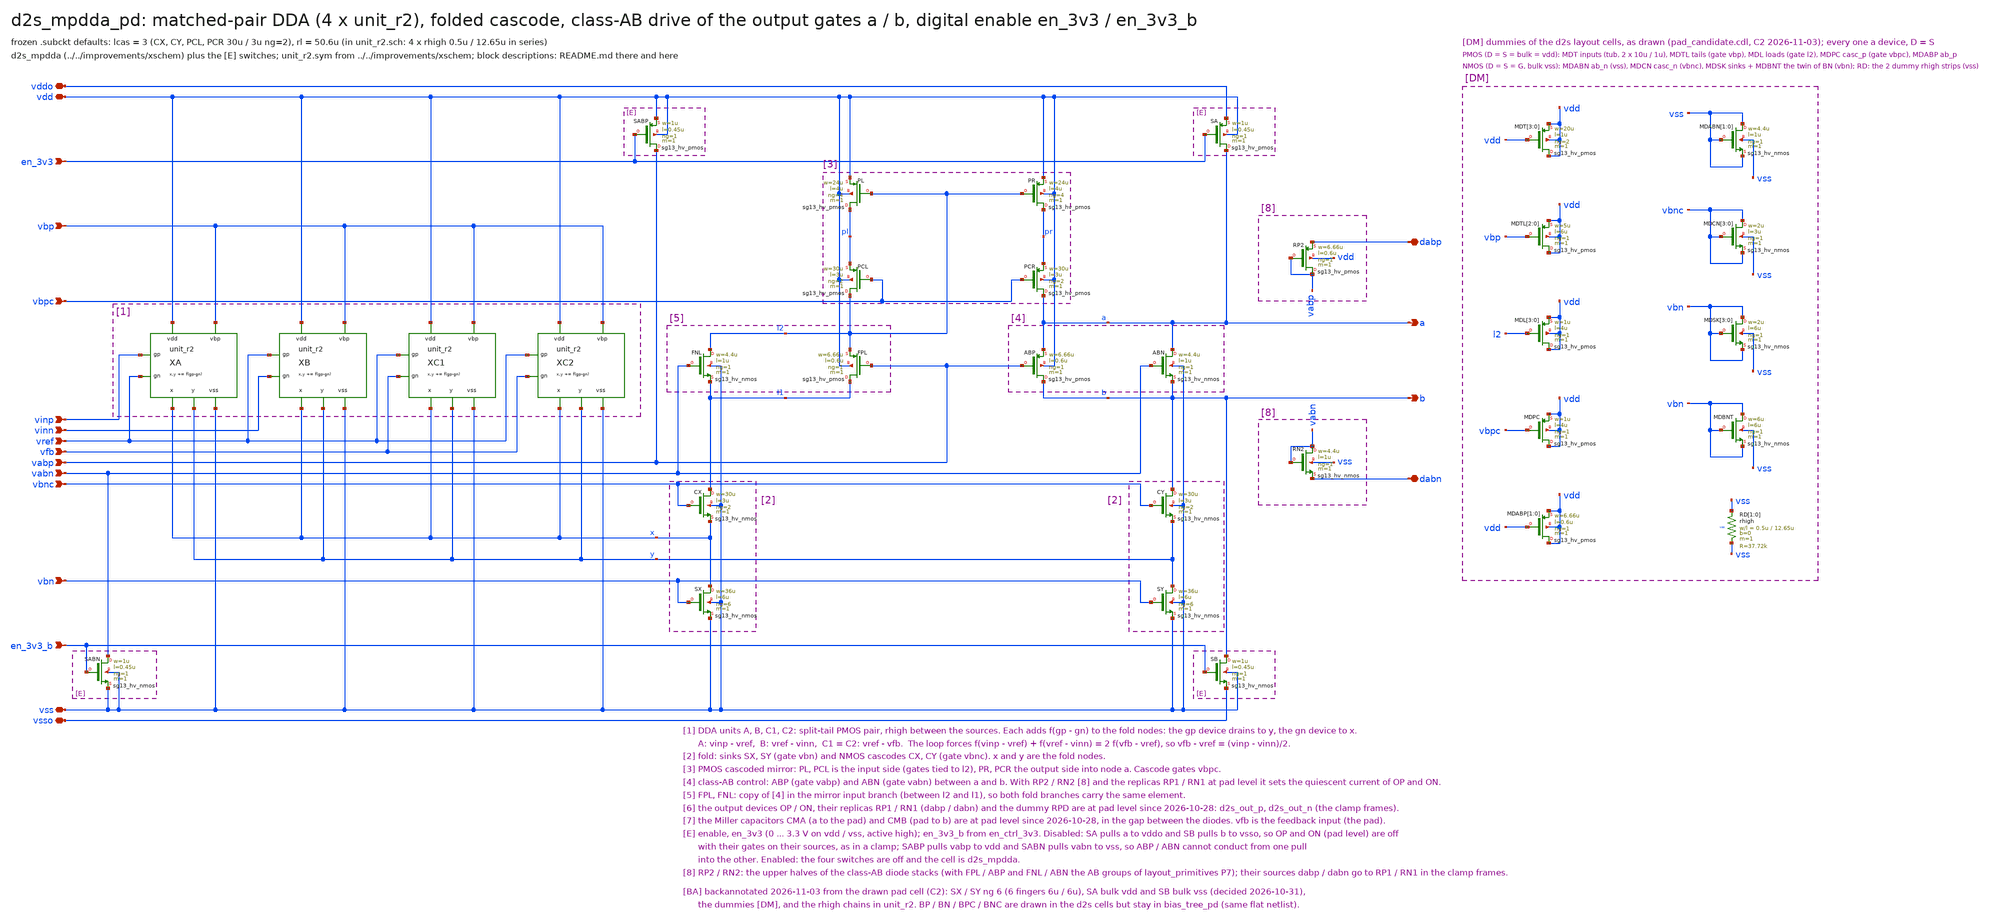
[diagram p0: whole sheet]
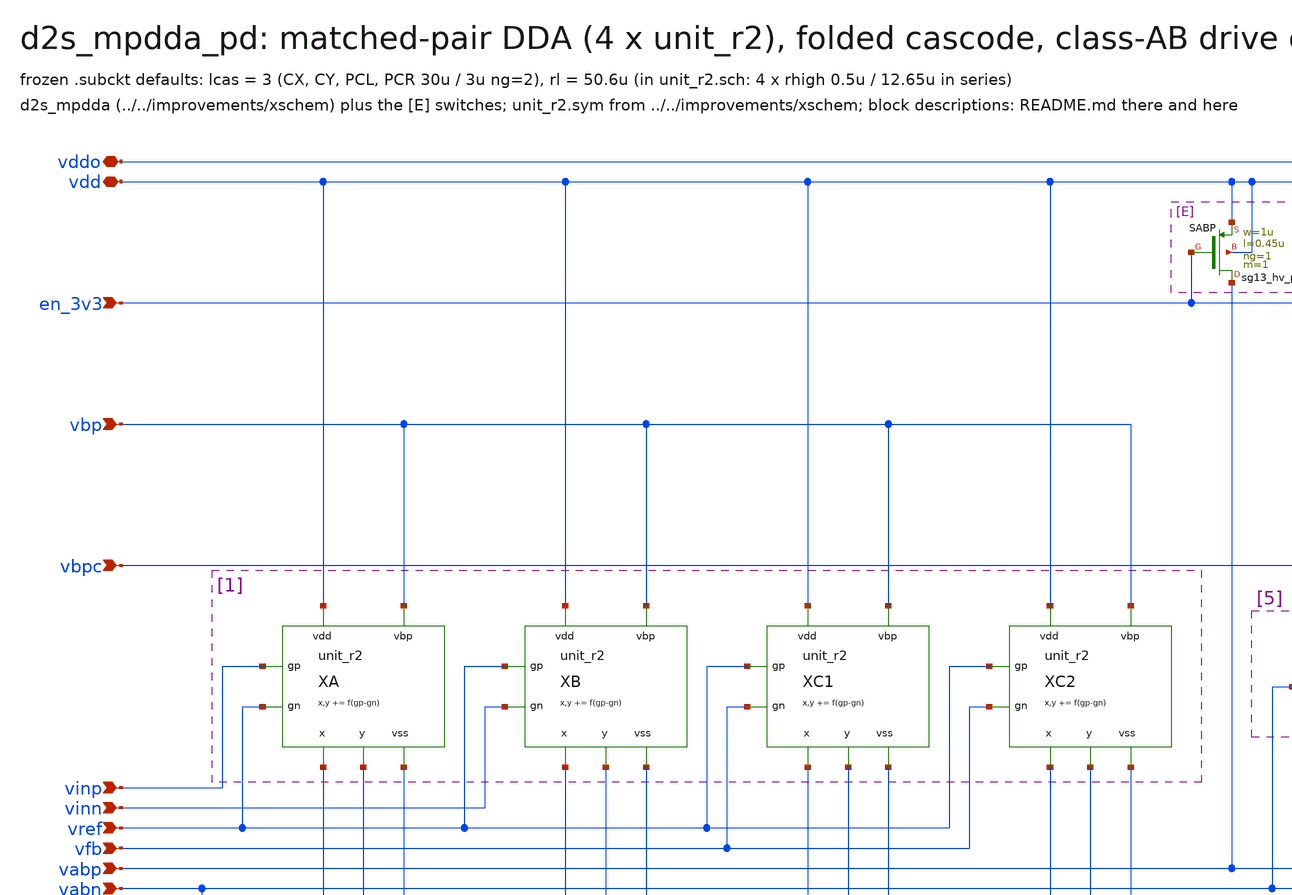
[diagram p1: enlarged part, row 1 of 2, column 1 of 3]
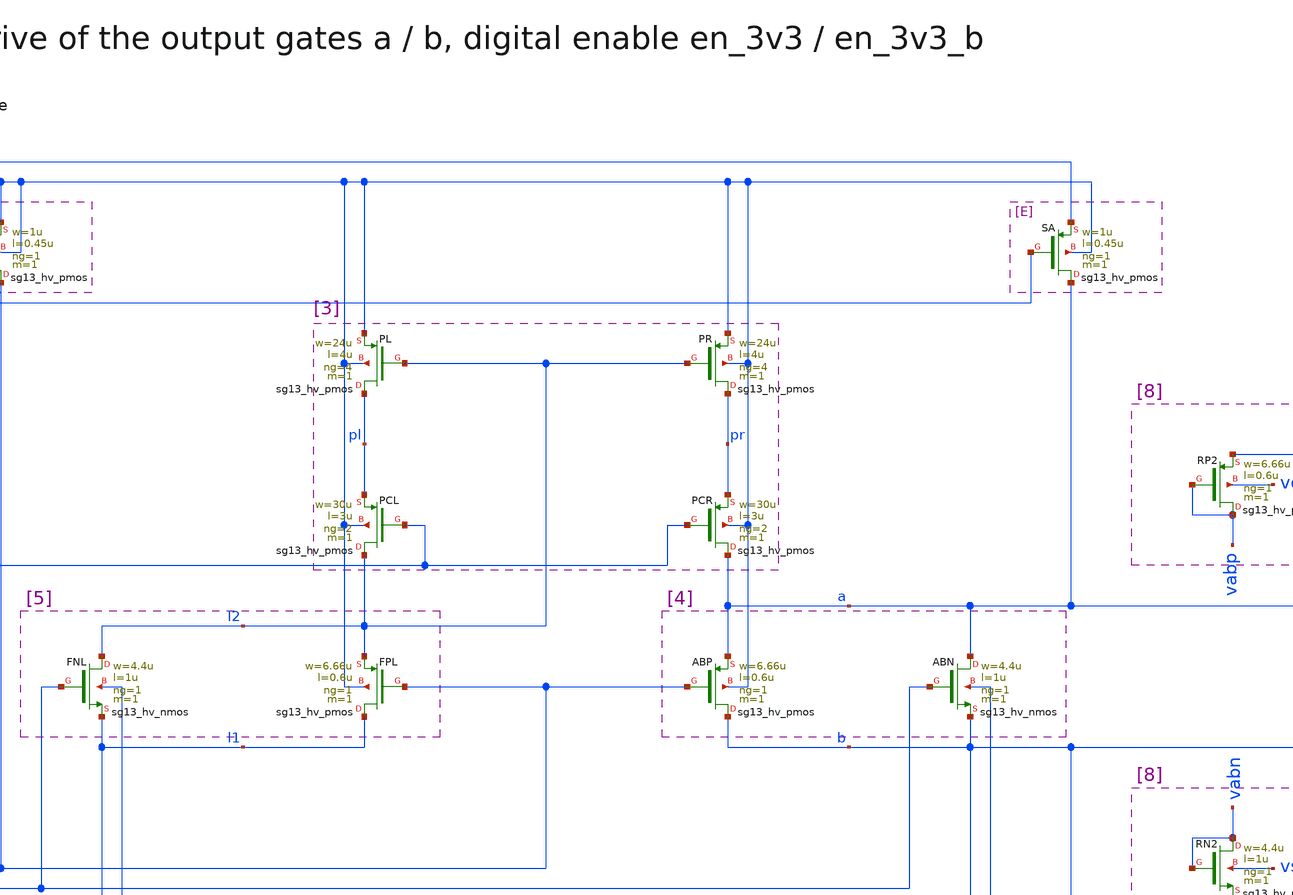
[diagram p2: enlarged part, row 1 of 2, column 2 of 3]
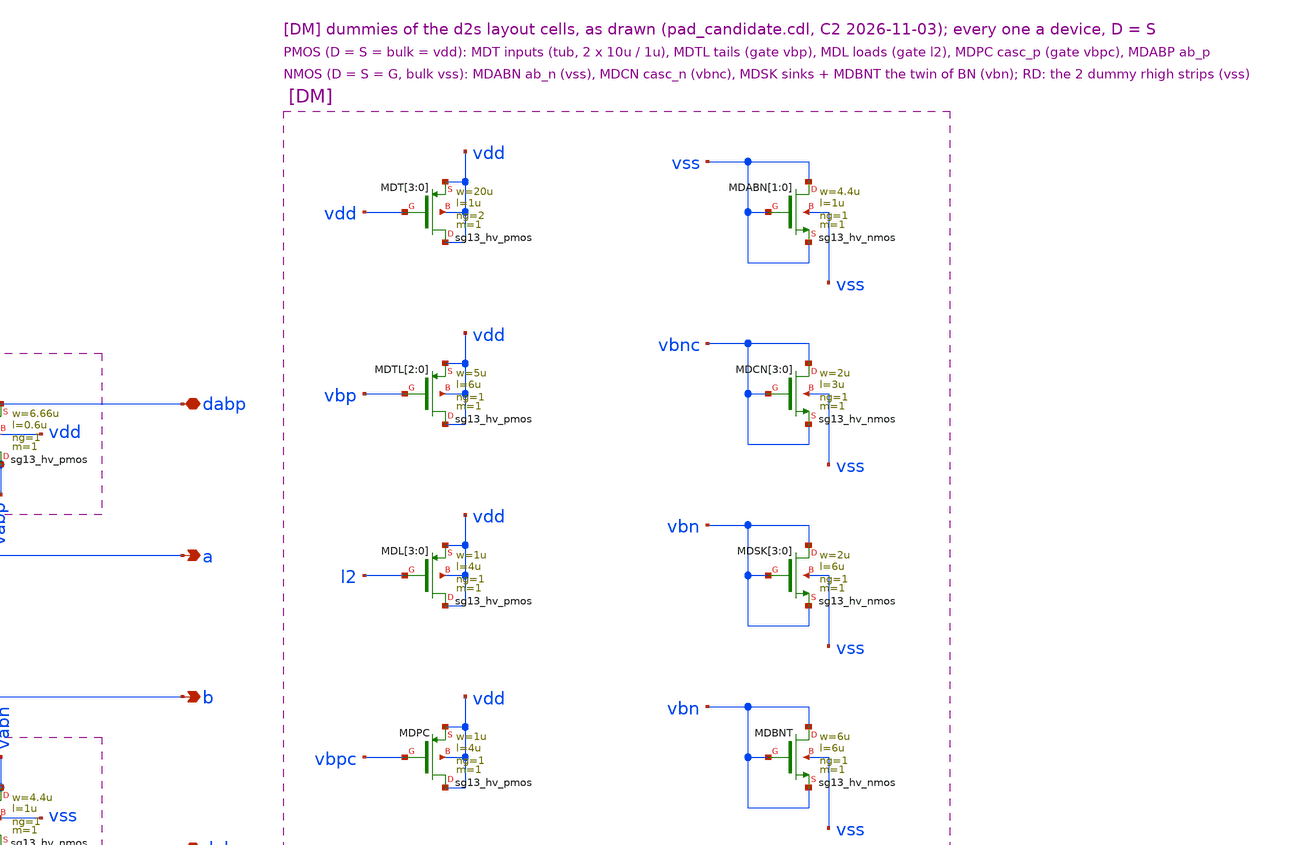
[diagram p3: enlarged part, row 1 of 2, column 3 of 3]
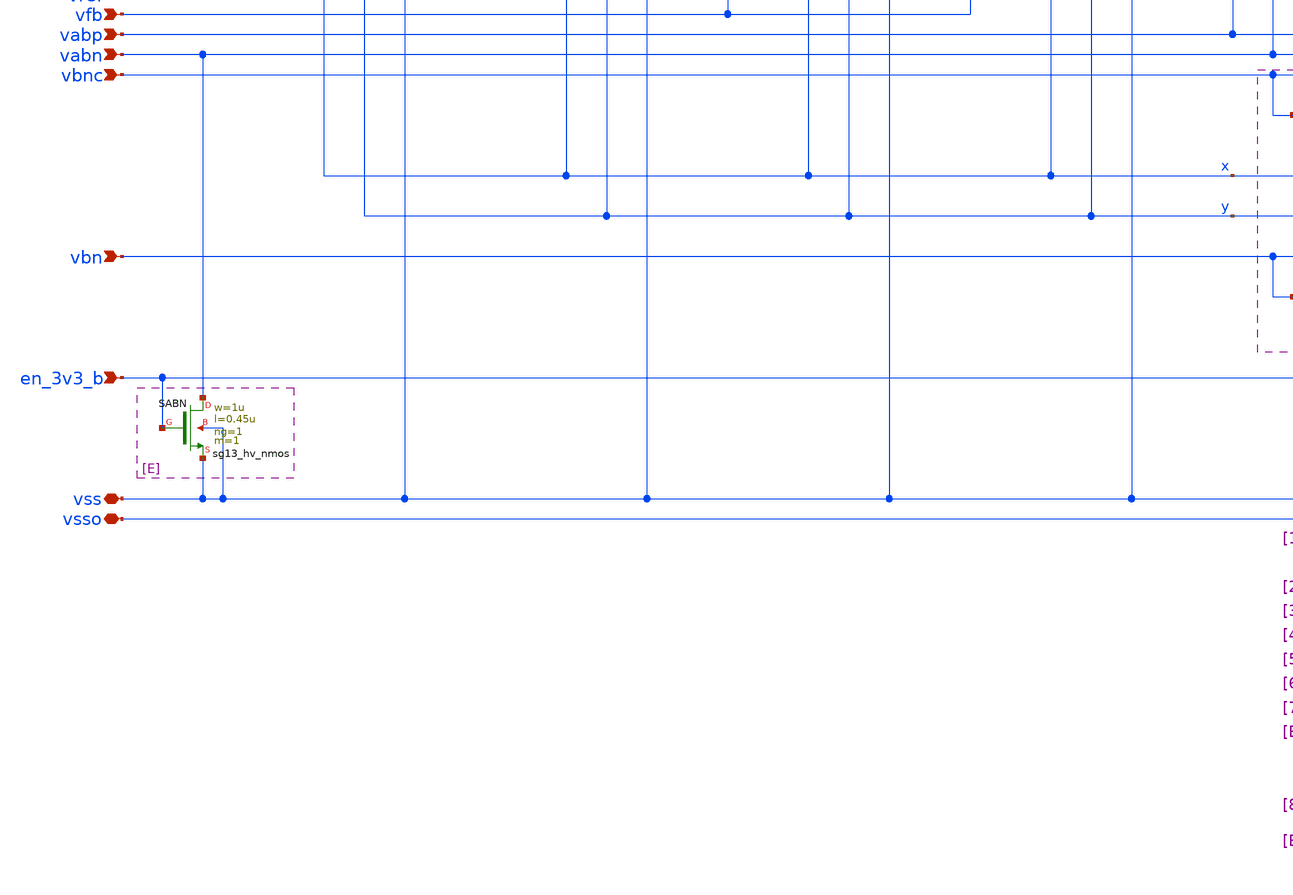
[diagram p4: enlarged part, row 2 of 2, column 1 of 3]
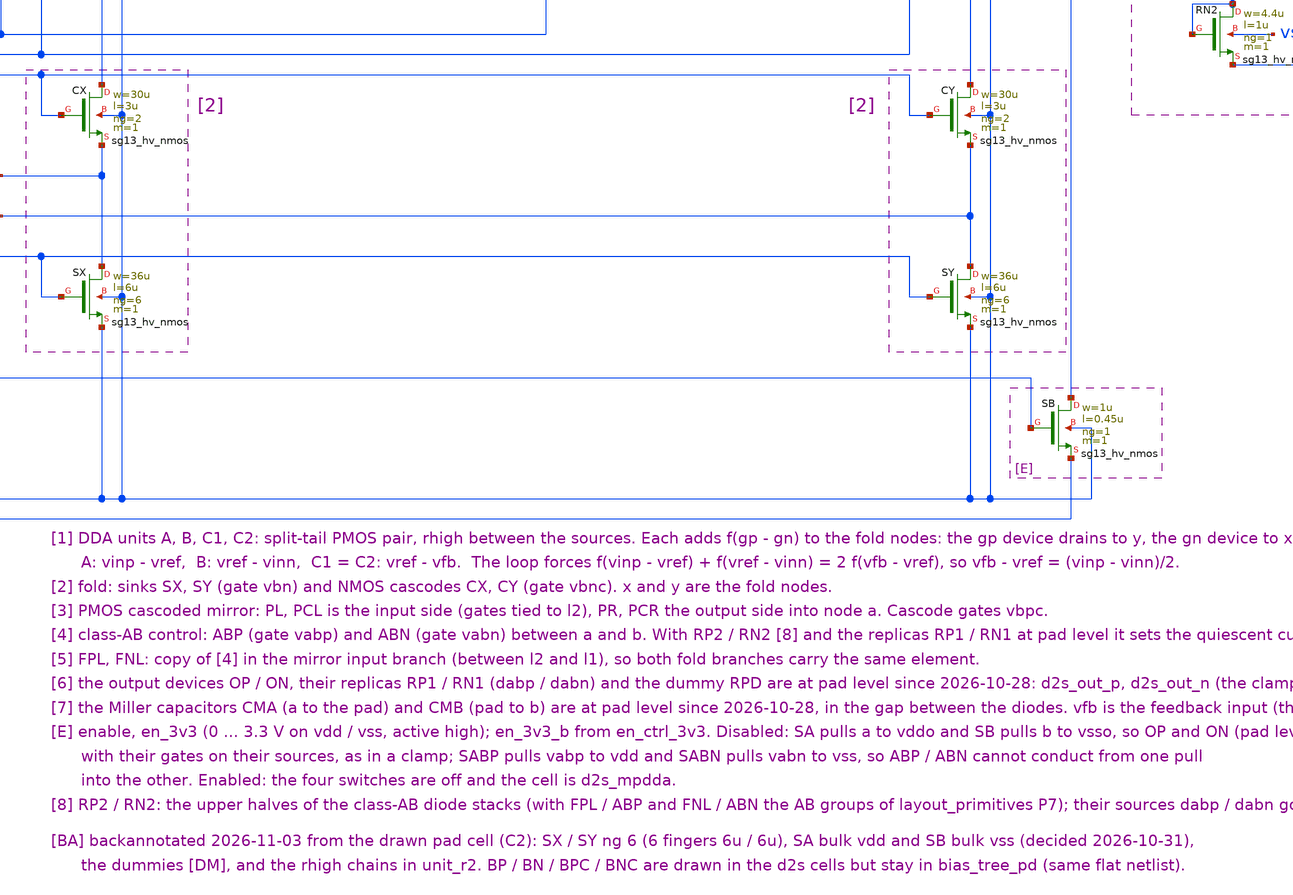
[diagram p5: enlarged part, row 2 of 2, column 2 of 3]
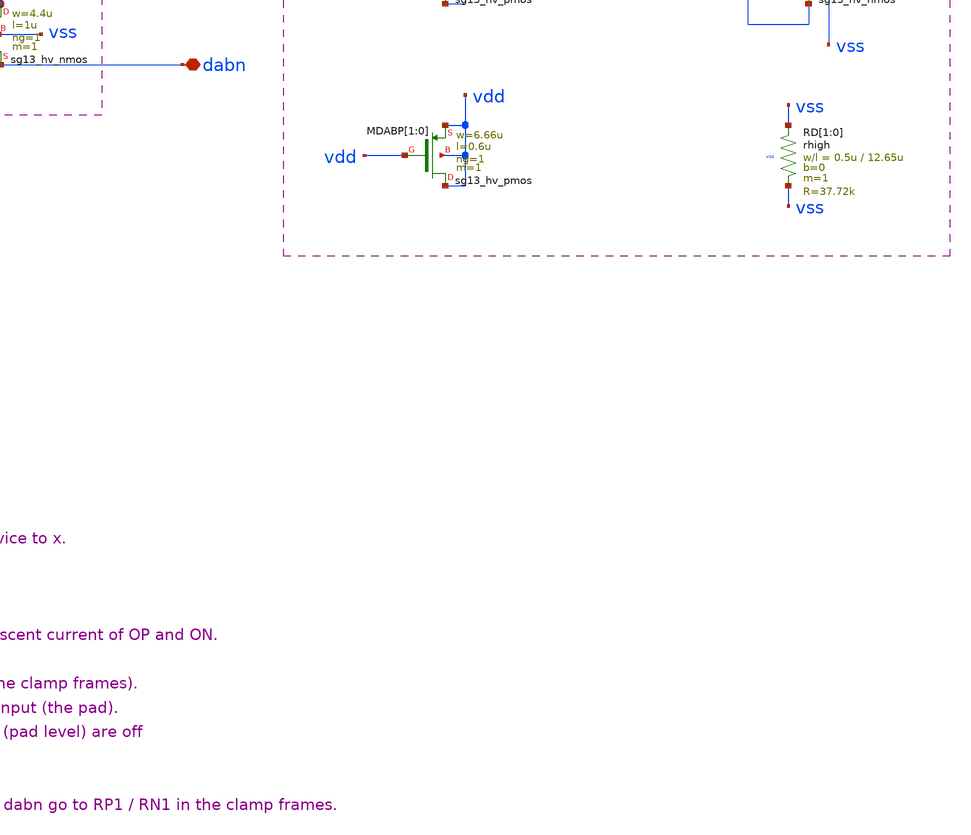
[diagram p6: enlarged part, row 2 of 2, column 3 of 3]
** sch_path: macros/sg13cmos5l_IOPadDiff2Single/schematic/xschem/d2s_mpdda_pd.sch
**.subckt d2s_mpdda_pd vdd vss vddo vsso vinp vinn vref vfb vbp vbn vbpc vbnc vabp vabn en_3v3
*+ en_3v3_b a b dabp dabn
*.iopin vdd
*.iopin vss
*.iopin vddo
*.iopin vsso
*.ipin vinp
*.ipin vinn
*.ipin vref
*.ipin vfb
*.ipin vbp
*.ipin vbn
*.ipin vbpc
*.ipin vbnc
*.ipin vabp
*.ipin vabn
*.ipin en_3v3
*.ipin en_3v3_b
*.opin a
*.opin b
*.iopin dabp
*.iopin dabn
XA x y vinp vref vdd vss vbp unit_r2
XB x y vref vinn vdd vss vbp unit_r2
XC1 x y vref vfb vdd vss vbp unit_r2
XC2 x y vref vfb vdd vss vbp unit_r2
XFNL l2 vabn l1 vss sg13_hv_nmos w=4.4u l=1u ng=1 m=1 mm_ok=1
XCX l1 vbnc x vss sg13_hv_nmos w=30u l=3u ng=2 m=1 mm_ok=1
XSX x vbn vss vss sg13_hv_nmos w=36u l=6u ng=6 m=1 mm_ok=1
XPL pl l2 vdd vdd sg13_hv_pmos w=24u l=4u ng=4 m=1 mm_ok=1
XPCL l2 vbpc pl vdd sg13_hv_pmos w=30u l=3u ng=2 m=1 mm_ok=1
XFPL l1 vabp l2 vdd sg13_hv_pmos w=6.66u l=0.6u ng=1 m=1 mm_ok=1
XPR pr l2 vdd vdd sg13_hv_pmos w=24u l=4u ng=4 m=1 mm_ok=1
XPCR a vbpc pr vdd sg13_hv_pmos w=30u l=3u ng=2 m=1 mm_ok=1
XABP b vabp a vdd sg13_hv_pmos w=6.66u l=0.6u ng=1 m=1 mm_ok=1
XABN a vabn b vss sg13_hv_nmos w=4.4u l=1u ng=1 m=1 mm_ok=1
XCY b vbnc y vss sg13_hv_nmos w=30u l=3u ng=2 m=1 mm_ok=1
XSY y vbn vss vss sg13_hv_nmos w=36u l=6u ng=6 m=1 mm_ok=1
XSABP vabp en_3v3 vdd vdd sg13_hv_pmos w=1u l=0.45u ng=1 m=1 mm_ok=1
XSA a en_3v3 vddo vdd sg13_hv_pmos w=1u l=0.45u ng=1 m=1 mm_ok=1
XSABN vabn en_3v3_b vss vss sg13_hv_nmos w=1u l=0.45u ng=1 m=1 mm_ok=1
XSB b en_3v3_b vsso vss sg13_hv_nmos w=1u l=0.45u ng=1 m=1 mm_ok=1
XRP2 vabp vabp dabp vdd sg13_hv_pmos w=6.66u l=0.6u ng=1 m=1 mm_ok=1
XRN2 vabn vabn dabn vss sg13_hv_nmos w=4.4u l=1u ng=1 m=1 mm_ok=1
XMDT[3] vdd vdd vdd vdd sg13_hv_pmos w=20u l=1u ng=2 m=1 mm_ok=1
XMDT[2] vdd vdd vdd vdd sg13_hv_pmos w=20u l=1u ng=2 m=1 mm_ok=1
XMDT[1] vdd vdd vdd vdd sg13_hv_pmos w=20u l=1u ng=2 m=1 mm_ok=1
XMDT[0] vdd vdd vdd vdd sg13_hv_pmos w=20u l=1u ng=2 m=1 mm_ok=1
XMDTL[2] vdd vbp vdd vdd sg13_hv_pmos w=5u l=6u ng=1 m=1 mm_ok=1
XMDTL[1] vdd vbp vdd vdd sg13_hv_pmos w=5u l=6u ng=1 m=1 mm_ok=1
XMDTL[0] vdd vbp vdd vdd sg13_hv_pmos w=5u l=6u ng=1 m=1 mm_ok=1
XMDL[3] vdd l2 vdd vdd sg13_hv_pmos w=1u l=4u ng=1 m=1 mm_ok=1
XMDL[2] vdd l2 vdd vdd sg13_hv_pmos w=1u l=4u ng=1 m=1 mm_ok=1
XMDL[1] vdd l2 vdd vdd sg13_hv_pmos w=1u l=4u ng=1 m=1 mm_ok=1
XMDL[0] vdd l2 vdd vdd sg13_hv_pmos w=1u l=4u ng=1 m=1 mm_ok=1
XMDPC vdd vbpc vdd vdd sg13_hv_pmos w=1u l=4u ng=1 m=1 mm_ok=1
XMDABP[1] vdd vdd vdd vdd sg13_hv_pmos w=6.66u l=0.6u ng=1 m=1 mm_ok=1
XMDABP[0] vdd vdd vdd vdd sg13_hv_pmos w=6.66u l=0.6u ng=1 m=1 mm_ok=1
XMDABN[1] vss vss vss vss sg13_hv_nmos w=4.4u l=1u ng=1 m=1 mm_ok=1
XMDABN[0] vss vss vss vss sg13_hv_nmos w=4.4u l=1u ng=1 m=1 mm_ok=1
XMDCN[3] vbnc vbnc vbnc vss sg13_hv_nmos w=2u l=3u ng=1 m=1 mm_ok=1
XMDCN[2] vbnc vbnc vbnc vss sg13_hv_nmos w=2u l=3u ng=1 m=1 mm_ok=1
XMDCN[1] vbnc vbnc vbnc vss sg13_hv_nmos w=2u l=3u ng=1 m=1 mm_ok=1
XMDCN[0] vbnc vbnc vbnc vss sg13_hv_nmos w=2u l=3u ng=1 m=1 mm_ok=1
XMDSK[3] vbn vbn vbn vss sg13_hv_nmos w=2u l=6u ng=1 m=1 mm_ok=1
XMDSK[2] vbn vbn vbn vss sg13_hv_nmos w=2u l=6u ng=1 m=1 mm_ok=1
XMDSK[1] vbn vbn vbn vss sg13_hv_nmos w=2u l=6u ng=1 m=1 mm_ok=1
XMDSK[0] vbn vbn vbn vss sg13_hv_nmos w=2u l=6u ng=1 m=1 mm_ok=1
XMDBNT vbn vbn vbn vss sg13_hv_nmos w=6u l=6u ng=1 m=1 mm_ok=1
XRD[1] vss vss vss rhigh w=0.5u l=12.65u m=1 b=0 mm_ok=1
XRD[0] vss vss vss rhigh w=0.5u l=12.65u m=1 b=0 mm_ok=1
**.ends

* expanding   symbol:  unit_r2.sym # of pins=7
** sym_path: sudelbuecher/design_considerations/class_ab_pad_driver/improvements/xschem/unit_r2.sym
** sch_path: sudelbuecher/design_considerations/class_ab_pad_driver/improvements/xschem/unit_r2.sch
.subckt unit_r2 x y gp gn vdd vss vbp
*.opin x
*.opin y
*.ipin gp
*.ipin gn
*.iopin vdd
*.iopin vss
*.ipin vbp
XTa sa vbp vdd vdd sg13_hv_pmos w=5u l=6u ng=1 m=1 mm_ok=1
XTb sb vbp vdd vdd sg13_hv_pmos w=5u l=6u ng=1 m=1 mm_ok=1
XMa y gp sa sa sg13_hv_pmos w=20u l=1u ng=2 m=1 mm_ok=1
XMb x gn sb sb sg13_hv_pmos w=20u l=1u ng=2 m=1 mm_ok=1
XR sa sb vss rhigh w=0.5u l=50.6u m=1 b=0 mm_ok=1
.ends

.end
